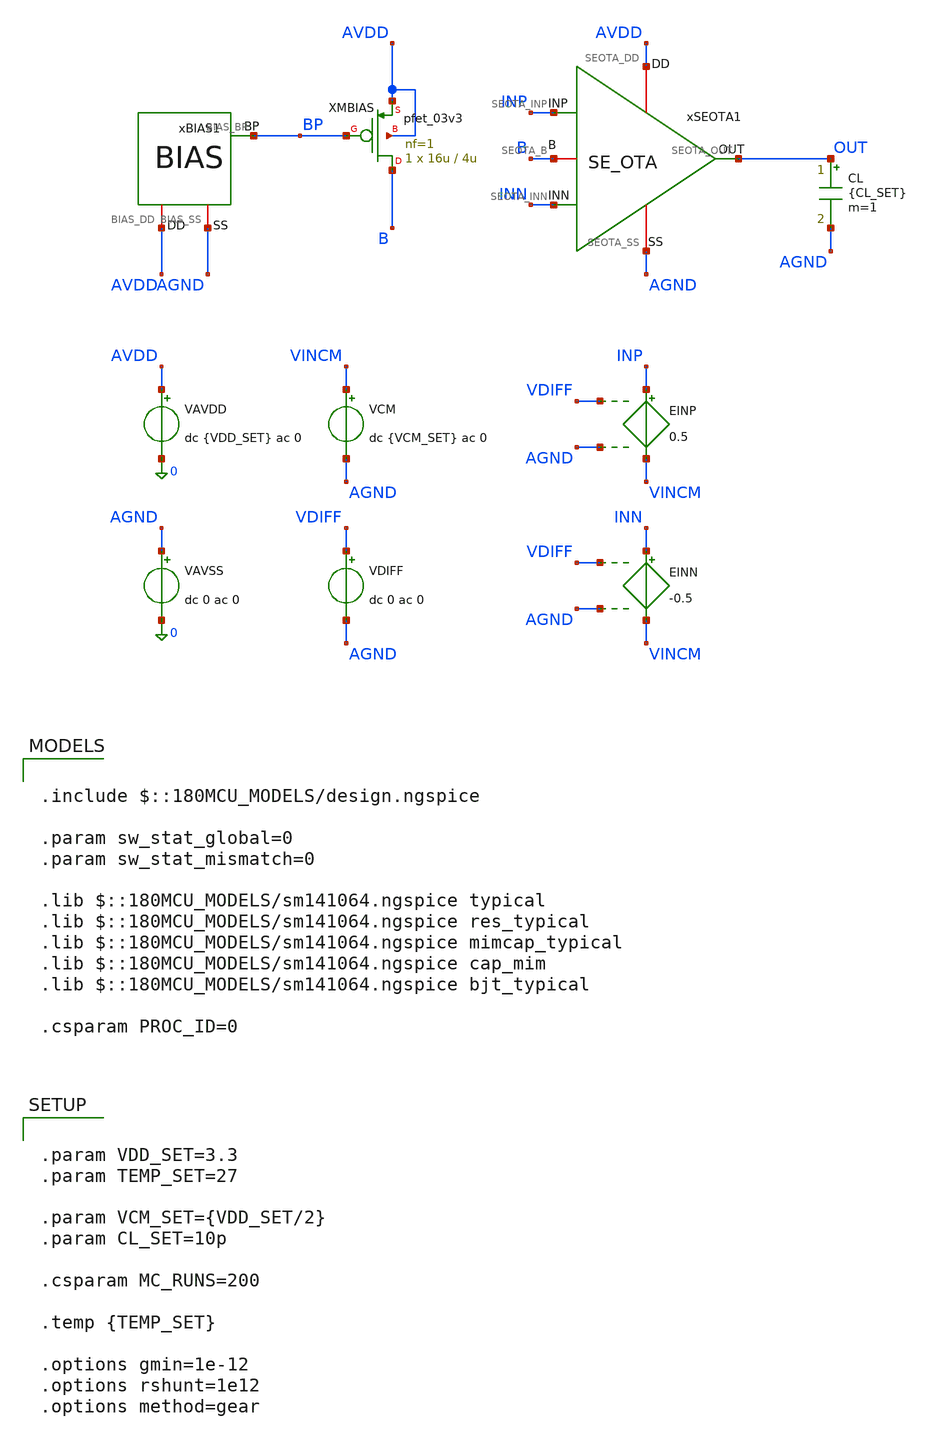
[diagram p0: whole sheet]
** sch_path: Design_Files/IC Design/Testbench/ANALOG_BLOCKS/SE_OTA/Open_Loop/SE_OTA_TB_OL_NOM.sch
**.subckt SE_OTA_TB_OL_NOM
VAVDD AVDD 0 dc {VDD_SET} ac 0
.save i(vavdd)
CL OUT AGND {CL_SET} m=1
VCM VINCM AGND dc {VCM_SET} ac 0
VDIFF VDIFF AGND dc 0 ac 0
xSEOTA1 AVDD AGND INP INN OUT B SE_OTA
VAVSS AGND 0 dc 0 ac 0
EINN INN VINCM VDIFF AGND -0.5
EINP INP VINCM VDIFF AGND 0.5
xBIAS1 AVDD AGND BP BIAS
XMBIAS B BP AVDD AVDD pfet_03v3 L=4u W=16u nf=1 ad='int((nf+1)/2) * W/nf * 0.18u' as='int((nf+2)/2) * W/nf * 0.18u'
+ pd='2*int((nf+1)/2) * (W/nf + 0.18u)' ps='2*int((nf+2)/2) * (W/nf + 0.18u)' nrd='0.18u / W' nrs='0.18u / W'
+ sa=0 sb=0 sd=0 m=1
**** begin user architecture code

.include $::180MCU_MODELS/design.ngspice

.param sw_stat_global=0
.param sw_stat_mismatch=0

.lib $::180MCU_MODELS/sm141064.ngspice typical
.lib $::180MCU_MODELS/sm141064.ngspice res_typical
.lib $::180MCU_MODELS/sm141064.ngspice mimcap_typical
.lib $::180MCU_MODELS/sm141064.ngspice cap_mim
.lib $::180MCU_MODELS/sm141064.ngspice bjt_typical

.csparam PROC_ID=0




.control

destroy all

set noaskquit
set wr_singlescale
unset wr_vecnames

option klu
option numdgt=15
option method=gear
option maxord=2
option plotwinsize=0


if $&PROC_ID = 0
set proc=NOM
else
if $&PROC_ID = 1
set proc=FF
else
if $&PROC_ID = 2
set proc=SS
else
if $&PROC_ID = 3
set proc=FS
else
set proc=SF
end
end
end
end


shell mkdir -p /foss/designs/ECG_Acquisition_IC/Measurement_Results/IC_Simulation/ANALOG_BLOCKS/SE_OTA/{$proc}.Result_txt
shell rm -f /foss/designs/ECG_Acquisition_IC/Measurement_Results/IC_Simulation/ANALOG_BLOCKS/SE_OTA/{$proc}.Result_txt/{$proc}.ol_*.txt


foreach vddval 3.3 3.0 3.6
foreach tval 27 -40 125


if $vddval = 3.3

if $tval = 27
set case=nom
else
if $tval = -40
set case=tl
else
set case=th
end
end

else

if $vddval = 3.0

if $tval = 27
set case=vl
else
if $tval = -40
set case=vltl
else
set case=vlth
end
end

else

if $tval = 27
set case=vh
else
if $tval = -40
set case=vhtl
else
set case=vhth
end
end

end
end


alterparam VDD_SET=$vddval
alterparam TEMP_SET=$tval

reset

option klu

save all
save @m.xmbias.m0[id]


* OP

op

let vdd=v(AVDD)-v(AGND)
let vinp=v(INP)-v(AGND)
let vinn=v(INN)-v(AGND)
let vout=v(OUT)-v(AGND)

let idd_total=abs(vavdd#branch)
let ibias=abs(@m.xmbias.m0[id])

wrdata /foss/designs/ECG_Acquisition_IC/Measurement_Results/IC_Simulation/ANALOG_BLOCKS/SE_OTA/{$proc}.Result_txt/{$proc}.ol_{$case}_op.txt
+ vdd vinp vinn vout v(B) idd_total ibias


* DIFFERENTIAL AC

alter @VCM[ACMAG]=0
alter @VDIFF[ACMAG]=1
alter @VDIFF[ACPHASE]=0
alter @VAVDD[ACMAG]=0
alter @VAVSS[ACMAG]=0

ac dec 200 0.01 1G

let vin_diff=v(INP)-v(INN)
let vout=v(OUT)-v(AGND)

let vin_diff_real=real(vin_diff)
let vin_diff_imag=imag(vin_diff)

let vout_real=real(vout)
let vout_imag=imag(vout)

setscale frequency

wrdata /foss/designs/ECG_Acquisition_IC/Measurement_Results/IC_Simulation/ANALOG_BLOCKS/SE_OTA/{$proc}.Result_txt/{$proc}.ol_{$case}_diff_ac.txt
+ vin_diff_real vin_diff_imag vout_real vout_imag


* COMMON-MODE AC

alter @VCM[ACMAG]=1
alter @VCM[ACPHASE]=0
alter @VDIFF[ACMAG]=0
alter @VAVDD[ACMAG]=0
alter @VAVSS[ACMAG]=0

ac dec 200 0.01 1G

let vin_cm=0.5*(v(INP)+v(INN))-v(AGND)
let vout=v(OUT)-v(AGND)

let vin_cm_real=real(vin_cm)
let vin_cm_imag=imag(vin_cm)

let vout_real=real(vout)
let vout_imag=imag(vout)

setscale frequency

wrdata /foss/designs/ECG_Acquisition_IC/Measurement_Results/IC_Simulation/ANALOG_BLOCKS/SE_OTA/{$proc}.Result_txt/{$proc}.ol_{$case}_cm_ac.txt
+ vin_cm_real vin_cm_imag vout_real vout_imag


* PSRRP

alter @VCM[ACMAG]=0
alter @VDIFF[ACMAG]=0
alter @VAVDD[ACMAG]=1
alter @VAVDD[ACPHASE]=0
alter @VAVSS[ACMAG]=0

ac dec 200 0.01 1G

let vsup=v(AVDD)-v(AGND)
let vout=v(OUT)-v(AGND)

let vsup_real=real(vsup)
let vsup_imag=imag(vsup)

let vout_real=real(vout)
let vout_imag=imag(vout)

setscale frequency

wrdata /foss/designs/ECG_Acquisition_IC/Measurement_Results/IC_Simulation/ANALOG_BLOCKS/SE_OTA/{$proc}.Result_txt/{$proc}.ol_{$case}_psrrp_ac.txt
+ vsup_real vsup_imag vout_real vout_imag


* PSRRN

alter @VCM[ACMAG]=0
alter @VDIFF[ACMAG]=0
alter @VAVDD[ACMAG]=0
alter @VAVSS[ACMAG]=1
alter @VAVSS[ACPHASE]=0

ac dec 200 0.01 1G

let vagnd=v(AGND)
let vout=v(OUT)-v(AGND)

let vagnd_real=real(vagnd)
let vagnd_imag=imag(vagnd)

let vout_real=real(vout)
let vout_imag=imag(vout)

setscale frequency

wrdata /foss/designs/ECG_Acquisition_IC/Measurement_Results/IC_Simulation/ANALOG_BLOCKS/SE_OTA/{$proc}.Result_txt/{$proc}.ol_{$case}_psrrn_ac.txt
+ vagnd_real vagnd_imag vout_real vout_imag


* VTC

alter @VCM[ACMAG]=0
alter @VDIFF[ACMAG]=0
alter @VAVDD[ACMAG]=0
alter @VAVSS[ACMAG]=0

dc VDIFF -20m 20m 1u

let vin_cm=0.5*(v(INP)+v(INN))-v(AGND)
let vin_diff=v(INP)-v(INN)
let vout=v(OUT)-v(AGND)

let idd_total=abs(vavdd#branch)

setscale vin_diff

wrdata /foss/designs/ECG_Acquisition_IC/Measurement_Results/IC_Simulation/ANALOG_BLOCKS/SE_OTA/{$proc}.Result_txt/{$proc}.ol_{$case}_vtc.txt
+ vin_cm v(INP) v(INN) vout idd_total


* NOISE

option sparse

alter @VCM[ACMAG]=0
alter @VDIFF[ACMAG]=1
alter @VDIFF[ACPHASE]=0
alter @VAVDD[ACMAG]=0
alter @VAVSS[ACMAG]=0

noise v(OUT) VDIFF dec 100 0.01 1k

setplot previous
setscale frequency

wrdata /foss/designs/ECG_Acquisition_IC/Measurement_Results/IC_Simulation/ANALOG_BLOCKS/SE_OTA/{$proc}.Result_txt/{$proc}.ol_{$case}_noise.txt
+ onoise_spectrum inoise_spectrum


destroy all

end
end


quit

.endc




.param VDD_SET=3.3
.param TEMP_SET=27

.param VCM_SET={VDD_SET/2}
.param CL_SET=10p

.csparam MC_RUNS=200

.temp {TEMP_SET}

.options gmin=1e-12
.options rshunt=1e12
.options method=gear


**** end user architecture code
**.ends

* expanding   symbol:  ECG_Acquisition_IC/Design_Files/IC
*+ Design/Schematic/ANALOG_BLOCKS/SE_OTA/SE_OTA.sym # of pins=6
** sym_path: Design_Files/IC Design/Schematic/SE_OTA/SE_OTA.sym
** sch_path: Design_Files/IC Design/Schematic/SE_OTA/SE_OTA.sch
.subckt SE_OTA SEOTA_DD SEOTA_SS SEOTA_INP SEOTA_INN SEOTA_OUT SEOTA_B
*.iopin SEOTA_DD
*.iopin SEOTA_SS
*.ipin SEOTA_INP
*.ipin SEOTA_INN
*.opin SEOTA_OUT
*.iopin SEOTA_B
XM3 net4 net4 SEOTA_DD SEOTA_DD pfet_03v3 L=4u W=1u nf=1 ad='int((nf+1)/2) * W/nf * 0.18u' as='int((nf+2)/2) * W/nf * 0.18u'
+ pd='2*int((nf+1)/2) * (W/nf + 0.18u)' ps='2*int((nf+2)/2) * (W/nf + 0.18u)' nrd='0.18u / W' nrs='0.18u / W'
+ sa=0 sb=0 sd=0 m=60
XM7 SEOTA_OUT SEOTA_B SEOTA_SS SEOTA_SS nfet_03v3 L=0.5u W=1u nf=1 ad='int((nf+1)/2) * W/nf * 0.18u'
+ as='int((nf+2)/2) * W/nf * 0.18u' pd='2*int((nf+1)/2) * (W/nf + 0.18u)' ps='2*int((nf+2)/2) * (W/nf + 0.18u)'
+ nrd='0.18u / W' nrs='0.18u / W' sa=0 sb=0 sd=0 m=100
Rz net1 net2 3.8k m=1
XM5 net3 SEOTA_B SEOTA_SS SEOTA_SS nfet_03v3 L=2u W=1u nf=1 ad='int((nf+1)/2) * W/nf * 0.18u' as='int((nf+2)/2) * W/nf * 0.18u'
+ pd='2*int((nf+1)/2) * (W/nf + 0.18u)' ps='2*int((nf+2)/2) * (W/nf + 0.18u)' nrd='0.18u / W' nrs='0.18u / W'
+ sa=0 sb=0 sd=0 m=10
XM6 SEOTA_OUT net1 SEOTA_DD SEOTA_DD pfet_03v3 L=0.5u W=1u nf=1 ad='int((nf+1)/2) * W/nf * 0.18u' as='int((nf+2)/2) * W/nf * 0.18u'
+ pd='2*int((nf+1)/2) * (W/nf + 0.18u)' ps='2*int((nf+2)/2) * (W/nf + 0.18u)' nrd='0.18u / W' nrs='0.18u / W'
+ sa=0 sb=0 sd=0 m=400
XM8 SEOTA_B SEOTA_B SEOTA_SS SEOTA_SS nfet_03v3 L=2u W=1u nf=1 ad='int((nf+1)/2) * W/nf * 0.18u' as='int((nf+2)/2) * W/nf * 0.18u'
+ pd='2*int((nf+1)/2) * (W/nf + 0.18u)' ps='2*int((nf+2)/2) * (W/nf + 0.18u)' nrd='0.18u / W' nrs='0.18u / W'
+ sa=0 sb=0 sd=0 m=20
Cc net2 SEOTA_OUT 2p m=1
XM4 net1 net4 SEOTA_DD SEOTA_DD pfet_03v3 L=4u W=1u nf=1 ad='int((nf+1)/2) * W/nf * 0.18u' as='int((nf+2)/2) * W/nf * 0.18u'
+ pd='2*int((nf+1)/2) * (W/nf + 0.18u)' ps='2*int((nf+2)/2) * (W/nf + 0.18u)' nrd='0.18u / W' nrs='0.18u / W'
+ sa=0 sb=0 sd=0 m=60
XM1 net4 SEOTA_INN net3 SEOTA_SS nfet_03v3 L=4u W=1u nf=1 ad='int((nf+1)/2) * W/nf * 0.18u' as='int((nf+2)/2) * W/nf * 0.18u'
+ pd='2*int((nf+1)/2) * (W/nf + 0.18u)' ps='2*int((nf+2)/2) * (W/nf + 0.18u)' nrd='0.18u / W' nrs='0.18u / W'
+ sa=0 sb=0 sd=0 m=400
XM2 net1 SEOTA_INP net3 SEOTA_SS nfet_03v3 L=4u W=1u nf=1 ad='int((nf+1)/2) * W/nf * 0.18u' as='int((nf+2)/2) * W/nf * 0.18u'
+ pd='2*int((nf+1)/2) * (W/nf + 0.18u)' ps='2*int((nf+2)/2) * (W/nf + 0.18u)' nrd='0.18u / W' nrs='0.18u / W'
+ sa=0 sb=0 sd=0 m=400
.ends


* expanding   symbol:  ECG_Acquisition_IC/Design_Files/IC Design/Schematic/AFE_BLOCKS/BIAS/BIAS.sym
*+ # of pins=3
** sym_path: Design_Files/IC Design/Schematic/AFE_BLOCKS/BIAS/BIAS.sym
** sch_path: Design_Files/IC Design/Schematic/AFE_BLOCKS/BIAS/BIAS.sch
.subckt BIAS BIAS_DD BIAS_SS BIAS_BP
*.iopin BIAS_DD
*.iopin BIAS_SS
*.opin BIAS_BP
XMN2 BIAS_BP net2 net1 BIAS_SS nfet_03v3 L=4u W=16u nf=1 ad='int((nf+1)/2) * W/nf * 0.18u' as='int((nf+2)/2) * W/nf * 0.18u'
+ pd='2*int((nf+1)/2) * (W/nf + 0.18u)' ps='2*int((nf+2)/2) * (W/nf + 0.18u)' nrd='0.18u / W' nrs='0.18u / W'
+ sa=0 sb=0 sd=0 m=1
XMP2 BIAS_BP BIAS_BP BIAS_DD BIAS_DD pfet_03v3 L=4u W=16u nf=1 ad='int((nf+1)/2) * W/nf * 0.18u' as='int((nf+2)/2) * W/nf * 0.18u'
+ pd='2*int((nf+1)/2) * (W/nf + 0.18u)' ps='2*int((nf+2)/2) * (W/nf + 0.18u)' nrd='0.18u / W' nrs='0.18u / W'
+ sa=0 sb=0 sd=0 m=1
XMN1 net2 net2 net3 BIAS_SS nfet_03v3 L=4u W=24u nf=1 ad='int((nf+1)/2) * W/nf * 0.18u' as='int((nf+2)/2) * W/nf * 0.18u'
+ pd='2*int((nf+1)/2) * (W/nf + 0.18u)' ps='2*int((nf+2)/2) * (W/nf + 0.18u)' nrd='0.18u / W' nrs='0.18u / W'
+ sa=0 sb=0 sd=0 m=1
XMP1 net2 BIAS_BP BIAS_DD BIAS_DD pfet_03v3 L=4u W=16u nf=1 ad='int((nf+1)/2) * W/nf * 0.18u' as='int((nf+2)/2) * W/nf * 0.18u'
+ pd='2*int((nf+1)/2) * (W/nf + 0.18u)' ps='2*int((nf+2)/2) * (W/nf + 0.18u)' nrd='0.18u / W' nrs='0.18u / W'
+ sa=0 sb=0 sd=0 m=1
XMST BIAS_BP BIAS_BP net2 BIAS_SS nfet_03v3 L=10u W=0.5u nf=1 ad='int((nf+1)/2) * W/nf * 0.18u' as='int((nf+2)/2) * W/nf * 0.18u'
+ pd='2*int((nf+1)/2) * (W/nf + 0.18u)' ps='2*int((nf+2)/2) * (W/nf + 0.18u)' nrd='0.18u / W' nrs='0.18u / W'
+ sa=0 sb=0 sd=0 m=1
XQ1 BIAS_SS BIAS_SS net3 pnp_05p00x00p42 m=1 par=1
XQ2 BIAS_SS BIAS_SS net4 pnp_05p00x00p42 m=30 par=30
XRS net4 net1 BIAS_SS nwell r_width=3e-6 r_length=1.522e-6 m=1
.ends

.end
